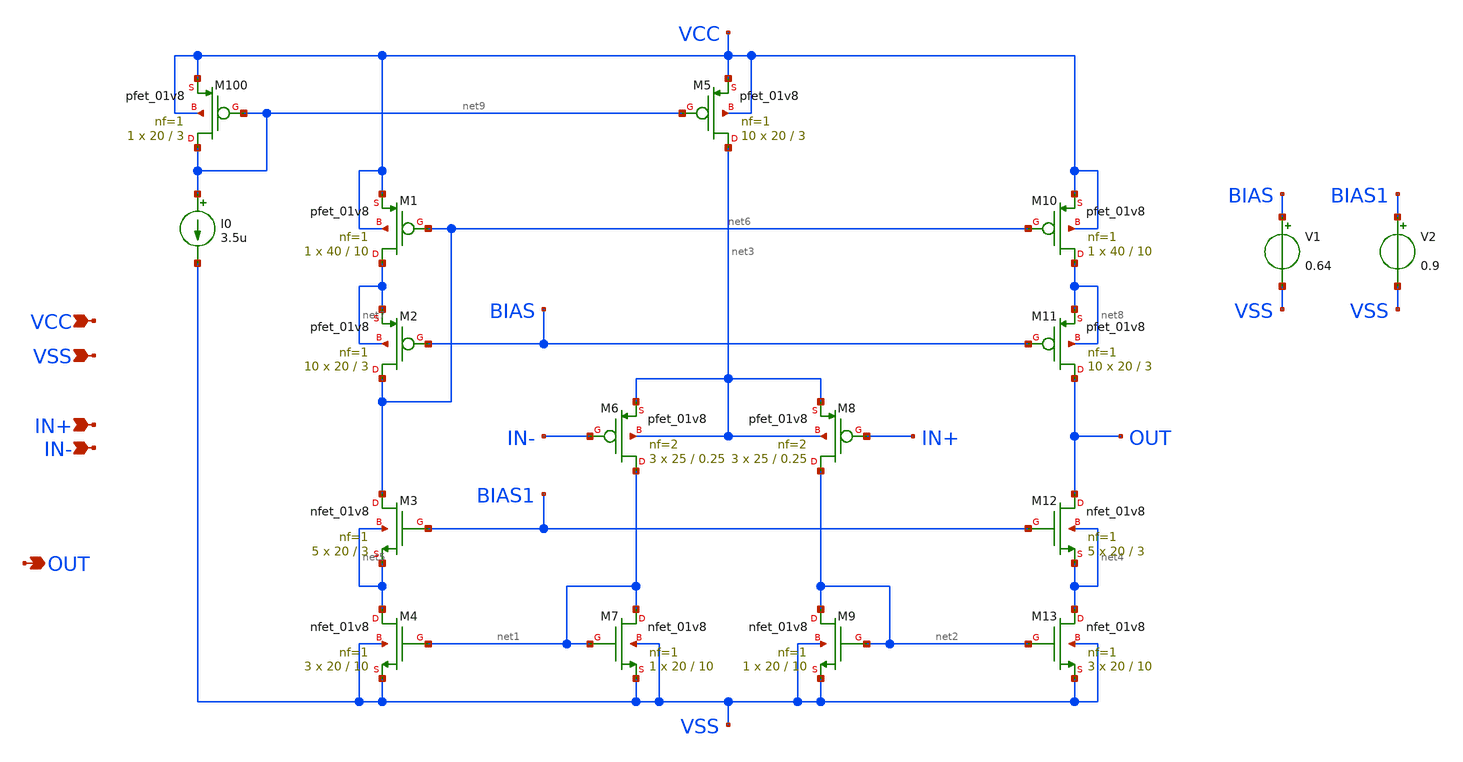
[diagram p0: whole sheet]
** sch_path: opamp_cascode.sch
**.subckt opamp_cascode IN+ IN- VCC VSS OUT
*.ipin IN+
*.ipin IN-
*.ipin VCC
*.ipin VSS
*.opin OUT
XM10 net8 net6 VCC VCC sky130_fd_pr__pfet_01v8 L=10 W=40 nf=1 ad='int((nf+1)/2) * W/nf * 0.29' as='int((nf+2)/2) * W/nf * 0.29'
+ pd='2*int((nf+1)/2) * (W/nf + 0.29)' ps='2*int((nf+2)/2) * (W/nf + 0.29)' nrd='0.29 / W' nrs='0.29 / W'
+ sa=0 sb=0 sd=0 mult=1 m=1
XM1 net7 net6 VCC VCC sky130_fd_pr__pfet_01v8 L=10 W=40 nf=1 ad='int((nf+1)/2) * W/nf * 0.29' as='int((nf+2)/2) * W/nf * 0.29'
+ pd='2*int((nf+1)/2) * (W/nf + 0.29)' ps='2*int((nf+2)/2) * (W/nf + 0.29)' nrd='0.29 / W' nrs='0.29 / W'
+ sa=0 sb=0 sd=0 mult=1 m=1
XM5 net3 net9 VCC VCC sky130_fd_pr__pfet_01v8 L=3 W=20 nf=1 ad='int((nf+1)/2) * W/nf * 0.29' as='int((nf+2)/2) * W/nf * 0.29'
+ pd='2*int((nf+1)/2) * (W/nf + 0.29)' ps='2*int((nf+2)/2) * (W/nf + 0.29)' nrd='0.29 / W' nrs='0.29 / W'
+ sa=0 sb=0 sd=0 mult=10 m=10
XM100 net9 net9 VCC VCC sky130_fd_pr__pfet_01v8 L=3 W=20 nf=1 ad='int((nf+1)/2) * W/nf * 0.29' as='int((nf+2)/2) * W/nf * 0.29'
+ pd='2*int((nf+1)/2) * (W/nf + 0.29)' ps='2*int((nf+2)/2) * (W/nf + 0.29)' nrd='0.29 / W' nrs='0.29 / W'
+ sa=0 sb=0 sd=0 mult=1 m=1
I0 net9 VSS 3.5u
XM11 OUT BIAS net8 net8 sky130_fd_pr__pfet_01v8 L=3 W=20 nf=1 ad='int((nf+1)/2) * W/nf * 0.29' as='int((nf+2)/2) * W/nf * 0.29'
+ pd='2*int((nf+1)/2) * (W/nf + 0.29)' ps='2*int((nf+2)/2) * (W/nf + 0.29)' nrd='0.29 / W' nrs='0.29 / W'
+ sa=0 sb=0 sd=0 mult=10 m=10
XM2 net6 BIAS net7 net7 sky130_fd_pr__pfet_01v8 L=3 W=20 nf=1 ad='int((nf+1)/2) * W/nf * 0.29' as='int((nf+2)/2) * W/nf * 0.29'
+ pd='2*int((nf+1)/2) * (W/nf + 0.29)' ps='2*int((nf+2)/2) * (W/nf + 0.29)' nrd='0.29 / W' nrs='0.29 / W'
+ sa=0 sb=0 sd=0 mult=10 m=10
XM6 net1 IN- net3 net3 sky130_fd_pr__pfet_01v8 L=0.25 W=25 nf=2 ad='int((nf+1)/2) * W/nf * 0.29' as='int((nf+2)/2) * W/nf * 0.29'
+ pd='2*int((nf+1)/2) * (W/nf + 0.29)' ps='2*int((nf+2)/2) * (W/nf + 0.29)' nrd='0.29 / W' nrs='0.29 / W'
+ sa=0 sb=0 sd=0 mult=3 m=3
XM8 net2 IN+ net3 net3 sky130_fd_pr__pfet_01v8 L=0.25 W=25 nf=2 ad='int((nf+1)/2) * W/nf * 0.29' as='int((nf+2)/2) * W/nf * 0.29'
+ pd='2*int((nf+1)/2) * (W/nf + 0.29)' ps='2*int((nf+2)/2) * (W/nf + 0.29)' nrd='0.29 / W' nrs='0.29 / W'
+ sa=0 sb=0 sd=0 mult=3 m=3
XM7 net1 net1 VSS VSS sky130_fd_pr__nfet_01v8 L=10 W=20 nf=1 ad='int((nf+1)/2) * W/nf * 0.29' as='int((nf+2)/2) * W/nf * 0.29'
+ pd='2*int((nf+1)/2) * (W/nf + 0.29)' ps='2*int((nf+2)/2) * (W/nf + 0.29)' nrd='0.29 / W' nrs='0.29 / W'
+ sa=0 sb=0 sd=0 mult=1 m=1
XM9 net2 net2 VSS VSS sky130_fd_pr__nfet_01v8 L=10 W=20 nf=1 ad='int((nf+1)/2) * W/nf * 0.29' as='int((nf+2)/2) * W/nf * 0.29'
+ pd='2*int((nf+1)/2) * (W/nf + 0.29)' ps='2*int((nf+2)/2) * (W/nf + 0.29)' nrd='0.29 / W' nrs='0.29 / W'
+ sa=0 sb=0 sd=0 mult=1 m=1
XM13 net4 net2 VSS VSS sky130_fd_pr__nfet_01v8 L=10 W=20 nf=1 ad='int((nf+1)/2) * W/nf * 0.29' as='int((nf+2)/2) * W/nf * 0.29'
+ pd='2*int((nf+1)/2) * (W/nf + 0.29)' ps='2*int((nf+2)/2) * (W/nf + 0.29)' nrd='0.29 / W' nrs='0.29 / W'
+ sa=0 sb=0 sd=0 mult=3 m=3
XM4 net5 net1 VSS VSS sky130_fd_pr__nfet_01v8 L=10 W=20 nf=1 ad='int((nf+1)/2) * W/nf * 0.29' as='int((nf+2)/2) * W/nf * 0.29'
+ pd='2*int((nf+1)/2) * (W/nf + 0.29)' ps='2*int((nf+2)/2) * (W/nf + 0.29)' nrd='0.29 / W' nrs='0.29 / W'
+ sa=0 sb=0 sd=0 mult=3 m=3
XM12 OUT BIAS1 net4 net4 sky130_fd_pr__nfet_01v8 L=3 W=20 nf=1 ad='int((nf+1)/2) * W/nf * 0.29' as='int((nf+2)/2) * W/nf * 0.29'
+ pd='2*int((nf+1)/2) * (W/nf + 0.29)' ps='2*int((nf+2)/2) * (W/nf + 0.29)' nrd='0.29 / W' nrs='0.29 / W'
+ sa=0 sb=0 sd=0 mult=5 m=5
XM3 net6 BIAS1 net5 net5 sky130_fd_pr__nfet_01v8 L=3 W=20 nf=1 ad='int((nf+1)/2) * W/nf * 0.29' as='int((nf+2)/2) * W/nf * 0.29'
+ pd='2*int((nf+1)/2) * (W/nf + 0.29)' ps='2*int((nf+2)/2) * (W/nf + 0.29)' nrd='0.29 / W' nrs='0.29 / W'
+ sa=0 sb=0 sd=0 mult=5 m=5
V1 BIAS VSS 0.64
V2 BIAS1 VSS 0.9
**.ends
.end
